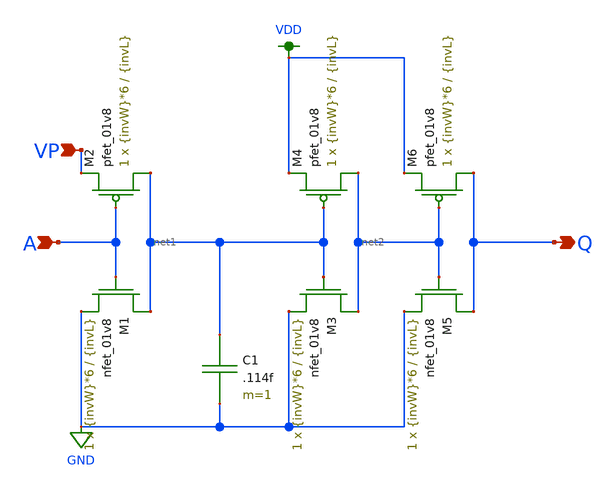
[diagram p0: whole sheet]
** sch_path: schemas/inv.sch
**.subckt inv A Q VP
*.ipin A
*.opin Q
*.ipin VP
XM1 net1 A GND GND sky130_fd_pr__nfet_01v8 L={invL} W={invW}*6 nf=1 ad='int((nf+1)/2) * W/nf * 0.29'
+ as='int((nf+2)/2) * W/nf * 0.29' pd='2*int((nf+1)/2) * (W/nf + 0.29)' ps='2*int((nf+2)/2) * (W/nf + 0.29)'
+ nrd='0.29 / W' nrs='0.29 / W' sa=0 sb=0 sd=0 mult=1 m=1
XM2 net1 A VP VDD sky130_fd_pr__pfet_01v8 L={invL} W={invW}*6 nf=1 ad='int((nf+1)/2) * W/nf * 0.29' as='int((nf+2)/2) * W/nf * 0.29'
+ pd='2*int((nf+1)/2) * (W/nf + 0.29)' ps='2*int((nf+2)/2) * (W/nf + 0.29)' nrd='0.29 / W' nrs='0.29 / W'
+ sa=0 sb=0 sd=0 mult=1 m=1
XM3 net2 net1 GND GND sky130_fd_pr__nfet_01v8 L={invL} W={invW}*6 nf=1 ad='int((nf+1)/2) * W/nf * 0.29'
+ as='int((nf+2)/2) * W/nf * 0.29' pd='2*int((nf+1)/2) * (W/nf + 0.29)' ps='2*int((nf+2)/2) * (W/nf + 0.29)'
+ nrd='0.29 / W' nrs='0.29 / W' sa=0 sb=0 sd=0 mult=1 m=1
XM4 net2 net1 VDD VDD sky130_fd_pr__pfet_01v8 L={invL} W={invW}*6 nf=1 ad='int((nf+1)/2) * W/nf * 0.29'
+ as='int((nf+2)/2) * W/nf * 0.29' pd='2*int((nf+1)/2) * (W/nf + 0.29)' ps='2*int((nf+2)/2) * (W/nf + 0.29)'
+ nrd='0.29 / W' nrs='0.29 / W' sa=0 sb=0 sd=0 mult=1 m=1
XM5 Q net2 GND GND sky130_fd_pr__nfet_01v8 L={invL} W={invW}*6 nf=1 ad='int((nf+1)/2) * W/nf * 0.29'
+ as='int((nf+2)/2) * W/nf * 0.29' pd='2*int((nf+1)/2) * (W/nf + 0.29)' ps='2*int((nf+2)/2) * (W/nf + 0.29)'
+ nrd='0.29 / W' nrs='0.29 / W' sa=0 sb=0 sd=0 mult=1 m=1
XM6 Q net2 VDD VDD sky130_fd_pr__pfet_01v8 L={invL} W={invW}*6 nf=1 ad='int((nf+1)/2) * W/nf * 0.29'
+ as='int((nf+2)/2) * W/nf * 0.29' pd='2*int((nf+1)/2) * (W/nf + 0.29)' ps='2*int((nf+2)/2) * (W/nf + 0.29)'
+ nrd='0.29 / W' nrs='0.29 / W' sa=0 sb=0 sd=0 mult=1 m=1
C1 net1 GND .114f m=1
**.ends
.GLOBAL GND
.GLOBAL VDD
.end
